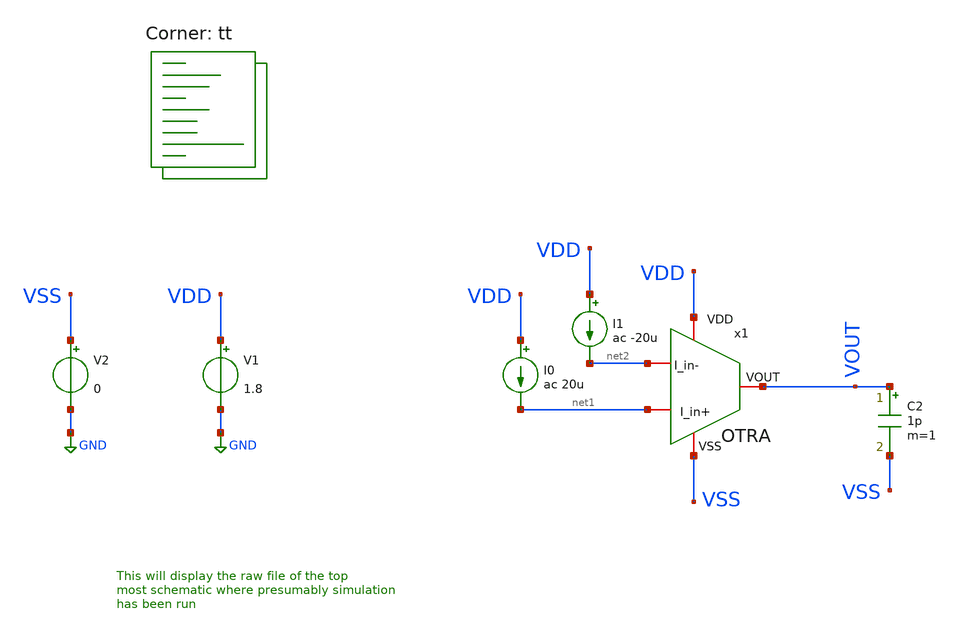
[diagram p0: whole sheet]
** sch_path: my_ip/testbenches_sky/OTRA_VGA/testbenches/tb.sch
**.subckt tb
V1 VDD GND 1.8
V2 VSS GND 0
x1 VDD VSS net2 net1 VOUT OTRA
C2 VOUT VSS 1p m=1
I0 VDD net1 ac 20u
I1 VDD net2 ac -20u
**** begin user architecture code
.lib $::SKYWATER_MODELS/sky130.lib.spice tt
**** end user architecture code
**.ends
.GLOBAL GND
**** begin user architecture code


* ngspice commands
.options savecurrents
.TEMP 27
.control
save all
save @m.x1.xm1.msky130_fd_pr__pfet_01v8_lvt[gm]
save @m.x1.xm1.msky130_fd_pr__pfet_01v8_lvt[vth]
save @m.x1.xm1.msky130_fd_pr__pfet_01v8_lvt[gds]
save @m.x1.xm1.msky130_fd_pr__pfet_01v8_lvt[gmbs]
save @m.x1.xm1.msky130_fd_pr__pfet_01v8_lvt[vds]
save @m.x1.xm1.msky130_fd_pr__pfet_01v8_lvt[vgs]


save @m.x1.xm2.msky130_fd_pr__pfet_01v8_lvt[gm]
save @m.x1.xm2.msky130_fd_pr__pfet_01v8_lvt[vth]
save @m.x1.xm2.msky130_fd_pr__pfet_01v8_lvt[gds]
save @m.x1.xm2.msky130_fd_pr__pfet_01v8_lvt[gmbs]
save @m.x1.xm2.msky130_fd_pr__pfet_01v8_lvt[vds]
save @m.x1.xm2.msky130_fd_pr__pfet_01v8_lvt[vgs]

save @m.x1.xm3.msky130_fd_pr__nfet_01v8[gm]
save @m.x1.xm3.msky130_fd_pr__nfet_01v8[vth]
save @m.x1.xm3.msky130_fd_pr__nfet_01v8[gds]
save @m.x1.xm3.msky130_fd_pr__nfet_01v8[gmbs]
save @m.x1.xm3.msky130_fd_pr__nfet_01v8[vds]
save @m.x1.xm3.msky130_fd_pr__nfet_01v8[vgs]

save @m.x1.xm4.msky130_fd_pr__nfet_01v8[gm]
save @m.x1.xm4.msky130_fd_pr__nfet_01v8[vth]
save @m.x1.xm4.msky130_fd_pr__nfet_01v8[gds]
save @m.x1.xm4.msky130_fd_pr__nfet_01v8[gmbs]
save @m.x1.xm4.msky130_fd_pr__nfet_01v8[vds]
save @m.x1.xm4.msky130_fd_pr__nfet_01v8[vgs]

save @m.x1.xm5.msky130_fd_pr__nfet_01v8_lvt[gm]
save @m.x1.xm5.msky130_fd_pr__nfet_01v8_lvt[vth]
save @m.x1.xm5.msky130_fd_pr__nfet_01v8_lvt[gds]
save @m.x1.xm5.msky130_fd_pr__nfet_01v8_lvt[gmbs]
save @m.x1.xm5.msky130_fd_pr__nfet_01v8_lvt[vds]
save @m.x1.xm5.msky130_fd_pr__nfet_01v8_lvt[vgs]

save @m.x1.xm6.msky130_fd_pr__nfet_01v8_lvt[gm]
save @m.x1.xm6.msky130_fd_pr__nfet_01v8_lvt[vth]
save @m.x1.xm6.msky130_fd_pr__nfet_01v8_lvt[gds]
save @m.x1.xm6.msky130_fd_pr__nfet_01v8_lvt[gmbs]
save @m.x1.xm6.msky130_fd_pr__nfet_01v8_lvt[vds]
save @m.x1.xm6.msky130_fd_pr__nfet_01v8_lvt[vgs]


save @m.x1.xm7.msky130_fd_pr__pfet_01v8_lvt[gm]
save @m.x1.xm7.msky130_fd_pr__pfet_01v8_lvt[vth]
save @m.x1.xm7.msky130_fd_pr__pfet_01v8_lvt[gds]
save @m.x1.xm7.msky130_fd_pr__pfet_01v8_lvt[gmbs]
save @m.x1.xm7.msky130_fd_pr__pfet_01v8_lvt[vds]
save @m.x1.xm7.msky130_fd_pr__pfet_01v8_lvt[vgs]

save @m.x1.xm8.msky130_fd_pr__nfet_01v8[gm]
save @m.x1.xm8.msky130_fd_pr__nfet_01v8[vth]
save @m.x1.xm8.msky130_fd_pr__nfet_01v8[gds]
save @m.x1.xm8.msky130_fd_pr__nfet_01v8[gmbs]
save @m.x1.xm8.msky130_fd_pr__nfet_01v8[vds]
save @m.x1.xm8.msky130_fd_pr__nfet_01v8[vgs]

save @m.x1.xm9.msky130_fd_pr__nfet_01v8[gm]
save @m.x1.xm9.msky130_fd_pr__nfet_01v8[vth]
save @m.x1.xm9.msky130_fd_pr__nfet_01v8[gds]
save @m.x1.xm9.msky130_fd_pr__nfet_01v8[gmbs]
save @m.x1.xm9.msky130_fd_pr__nfet_01v8[vds]
save @m.x1.xm9.msky130_fd_pr__nfet_01v8[vgs]

save @m.x1.xm10.msky130_fd_pr__nfet_01v8_lvt[gm]
save @m.x1.xm10.msky130_fd_pr__nfet_01v8_lvt[vth]
save @m.x1.xm10.msky130_fd_pr__nfet_01v8_lvt[gds]
save @m.x1.xm10.msky130_fd_pr__nfet_01v8_lvt[gmbs]
save @m.x1.xm10.msky130_fd_pr__nfet_01v8_lvt[vds]
save @m.x1.xm10.msky130_fd_pr__nfet_01v8_lvt[vgs]

save @m.x1.xm11.msky130_fd_pr__pfet_01v8_lvt[gm]
save @m.x1.xm11.msky130_fd_pr__pfet_01v8_lvt[vth]
save @m.x1.xm11.msky130_fd_pr__pfet_01v8_lvt[gds]
save @m.x1.xm11.msky130_fd_pr__pfet_01v8_lvt[gmbs]
save @m.x1.xm11.msky130_fd_pr__pfet_01v8_lvt[vds]
save @m.x1.xm11.msky130_fd_pr__pfet_01v8_lvt[vgs]

save @m.x1.xm12.msky130_fd_pr__pfet_01v8_lvt[gm]
save @m.x1.xm12.msky130_fd_pr__pfet_01v8_lvt[vth]
save @m.x1.xm12.msky130_fd_pr__pfet_01v8_lvt[gds]
save @m.x1.xm12.msky130_fd_pr__pfet_01v8_lvt[gmbs]
save @m.x1.xm12.msky130_fd_pr__pfet_01v8_lvt[vds]
save @m.x1.xm12.msky130_fd_pr__pfet_01v8_lvt[vgs]
op
write tb.raw
ac dec 10 1 50G
plot db(v(VOUT)) (180*ph(v(VOUT))/pi)
.endc



**** end user architecture code
.end
